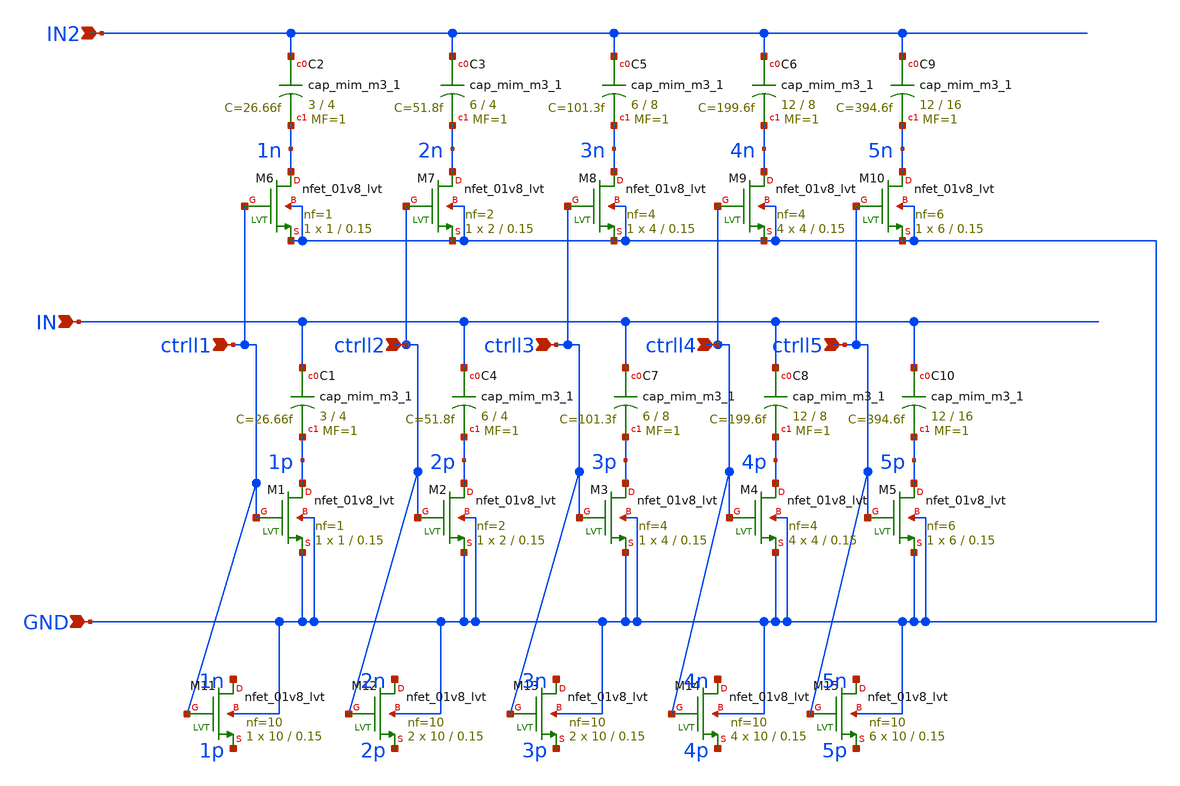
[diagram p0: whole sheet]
** sch_path: xschem/vco/cap_bank2.sch
**.subckt cap_bank2 IN GND ctrll1 ctrll2 ctrll3 ctrll4 ctrll5 IN2
*.ipin IN
*.ipin GND
*.ipin ctrll1
*.ipin ctrll2
*.ipin ctrll3
*.ipin ctrll4
*.ipin ctrll5
*.ipin IN2
XM11 1n ctrll1 1p GND sky130_fd_pr__nfet_01v8_lvt L=0.15 W=10 nf=10 ad='int((nf+1)/2) * W/nf * 0.29'
+ as='int((nf+2)/2) * W/nf * 0.29' pd='2*int((nf+1)/2) * (W/nf + 0.29)' ps='2*int((nf+2)/2) * (W/nf + 0.29)'
+ nrd='0.29 / W' nrs='0.29 / W' sa=0 sb=0 sd=0 mult=1 m=1
XM12 2n ctrll2 2p GND sky130_fd_pr__nfet_01v8_lvt L=0.15 W=10 nf=10 ad='int((nf+1)/2) * W/nf * 0.29'
+ as='int((nf+2)/2) * W/nf * 0.29' pd='2*int((nf+1)/2) * (W/nf + 0.29)' ps='2*int((nf+2)/2) * (W/nf + 0.29)'
+ nrd='0.29 / W' nrs='0.29 / W' sa=0 sb=0 sd=0 mult=2 m=2
XM13 3n ctrll3 3p GND sky130_fd_pr__nfet_01v8_lvt L=0.15 W=10 nf=10 ad='int((nf+1)/2) * W/nf * 0.29'
+ as='int((nf+2)/2) * W/nf * 0.29' pd='2*int((nf+1)/2) * (W/nf + 0.29)' ps='2*int((nf+2)/2) * (W/nf + 0.29)'
+ nrd='0.29 / W' nrs='0.29 / W' sa=0 sb=0 sd=0 mult=2 m=2
XM14 4n ctrll4 4p GND sky130_fd_pr__nfet_01v8_lvt L=0.15 W=10 nf=10 ad='int((nf+1)/2) * W/nf * 0.29'
+ as='int((nf+2)/2) * W/nf * 0.29' pd='2*int((nf+1)/2) * (W/nf + 0.29)' ps='2*int((nf+2)/2) * (W/nf + 0.29)'
+ nrd='0.29 / W' nrs='0.29 / W' sa=0 sb=0 sd=0 mult=4 m=4
XM15 5n ctrll5 5p GND sky130_fd_pr__nfet_01v8_lvt L=0.15 W=10 nf=10 ad='int((nf+1)/2) * W/nf * 0.29'
+ as='int((nf+2)/2) * W/nf * 0.29' pd='2*int((nf+1)/2) * (W/nf + 0.29)' ps='2*int((nf+2)/2) * (W/nf + 0.29)'
+ nrd='0.29 / W' nrs='0.29 / W' sa=0 sb=0 sd=0 mult=6 m=6
XC2 IN2 1n sky130_fd_pr__cap_mim_m3_1 W=3 L=4 MF=1 m=1
XC3 IN2 2n sky130_fd_pr__cap_mim_m3_1 W=6 L=4 MF=1 m=1
XC5 IN2 3n sky130_fd_pr__cap_mim_m3_1 W=6 L=8 MF=1 m=1
XC6 IN2 4n sky130_fd_pr__cap_mim_m3_1 W=12 L=8 MF=1 m=1
XC9 IN2 5n sky130_fd_pr__cap_mim_m3_1 W=12 L=16 MF=1 m=1
XM1 1p ctrll1 GND GND sky130_fd_pr__nfet_01v8_lvt L=0.15 W=1 nf=1 ad='int((nf+1)/2) * W/nf * 0.29' as='int((nf+2)/2) * W/nf * 0.29'
+ pd='2*int((nf+1)/2) * (W/nf + 0.29)' ps='2*int((nf+2)/2) * (W/nf + 0.29)' nrd='0.29 / W' nrs='0.29 / W'
+ sa=0 sb=0 sd=0 mult=1 m=1
XM2 2p ctrll2 GND GND sky130_fd_pr__nfet_01v8_lvt L=0.15 W=2 nf=2 ad='int((nf+1)/2) * W/nf * 0.29' as='int((nf+2)/2) * W/nf * 0.29'
+ pd='2*int((nf+1)/2) * (W/nf + 0.29)' ps='2*int((nf+2)/2) * (W/nf + 0.29)' nrd='0.29 / W' nrs='0.29 / W'
+ sa=0 sb=0 sd=0 mult=1 m=1
XM3 3p ctrll3 GND GND sky130_fd_pr__nfet_01v8_lvt L=0.15 W=4 nf=4 ad='int((nf+1)/2) * W/nf * 0.29' as='int((nf+2)/2) * W/nf * 0.29'
+ pd='2*int((nf+1)/2) * (W/nf + 0.29)' ps='2*int((nf+2)/2) * (W/nf + 0.29)' nrd='0.29 / W' nrs='0.29 / W'
+ sa=0 sb=0 sd=0 mult=1 m=1
XM4 4p ctrll4 GND GND sky130_fd_pr__nfet_01v8_lvt L=0.15 W=4 nf=4 ad='int((nf+1)/2) * W/nf * 0.29' as='int((nf+2)/2) * W/nf * 0.29'
+ pd='2*int((nf+1)/2) * (W/nf + 0.29)' ps='2*int((nf+2)/2) * (W/nf + 0.29)' nrd='0.29 / W' nrs='0.29 / W'
+ sa=0 sb=0 sd=0 mult=4 m=4
XM5 5p ctrll5 GND GND sky130_fd_pr__nfet_01v8_lvt L=0.15 W=6 nf=6 ad='int((nf+1)/2) * W/nf * 0.29' as='int((nf+2)/2) * W/nf * 0.29'
+ pd='2*int((nf+1)/2) * (W/nf + 0.29)' ps='2*int((nf+2)/2) * (W/nf + 0.29)' nrd='0.29 / W' nrs='0.29 / W'
+ sa=0 sb=0 sd=0 mult=1 m=1
XM6 1n ctrll1 GND GND sky130_fd_pr__nfet_01v8_lvt L=0.15 W=1 nf=1 ad='int((nf+1)/2) * W/nf * 0.29' as='int((nf+2)/2) * W/nf * 0.29'
+ pd='2*int((nf+1)/2) * (W/nf + 0.29)' ps='2*int((nf+2)/2) * (W/nf + 0.29)' nrd='0.29 / W' nrs='0.29 / W'
+ sa=0 sb=0 sd=0 mult=1 m=1
XM7 2n ctrll2 GND GND sky130_fd_pr__nfet_01v8_lvt L=0.15 W=2 nf=2 ad='int((nf+1)/2) * W/nf * 0.29' as='int((nf+2)/2) * W/nf * 0.29'
+ pd='2*int((nf+1)/2) * (W/nf + 0.29)' ps='2*int((nf+2)/2) * (W/nf + 0.29)' nrd='0.29 / W' nrs='0.29 / W'
+ sa=0 sb=0 sd=0 mult=1 m=1
XM8 3n ctrll3 GND GND sky130_fd_pr__nfet_01v8_lvt L=0.15 W=4 nf=4 ad='int((nf+1)/2) * W/nf * 0.29' as='int((nf+2)/2) * W/nf * 0.29'
+ pd='2*int((nf+1)/2) * (W/nf + 0.29)' ps='2*int((nf+2)/2) * (W/nf + 0.29)' nrd='0.29 / W' nrs='0.29 / W'
+ sa=0 sb=0 sd=0 mult=1 m=1
XM9 4n ctrll4 GND GND sky130_fd_pr__nfet_01v8_lvt L=0.15 W=4 nf=4 ad='int((nf+1)/2) * W/nf * 0.29' as='int((nf+2)/2) * W/nf * 0.29'
+ pd='2*int((nf+1)/2) * (W/nf + 0.29)' ps='2*int((nf+2)/2) * (W/nf + 0.29)' nrd='0.29 / W' nrs='0.29 / W'
+ sa=0 sb=0 sd=0 mult=4 m=4
XM10 5n ctrll5 GND GND sky130_fd_pr__nfet_01v8_lvt L=0.15 W=6 nf=6 ad='int((nf+1)/2) * W/nf * 0.29' as='int((nf+2)/2) * W/nf * 0.29'
+ pd='2*int((nf+1)/2) * (W/nf + 0.29)' ps='2*int((nf+2)/2) * (W/nf + 0.29)' nrd='0.29 / W' nrs='0.29 / W'
+ sa=0 sb=0 sd=0 mult=1 m=1
XC1 IN 1p sky130_fd_pr__cap_mim_m3_1 W=3 L=4 MF=1 m=1
XC4 IN 2p sky130_fd_pr__cap_mim_m3_1 W=6 L=4 MF=1 m=1
XC7 IN 3p sky130_fd_pr__cap_mim_m3_1 W=6 L=8 MF=1 m=1
XC8 IN 4p sky130_fd_pr__cap_mim_m3_1 W=12 L=8 MF=1 m=1
XC10 IN 5p sky130_fd_pr__cap_mim_m3_1 W=12 L=16 MF=1 m=1
**.ends
.end
